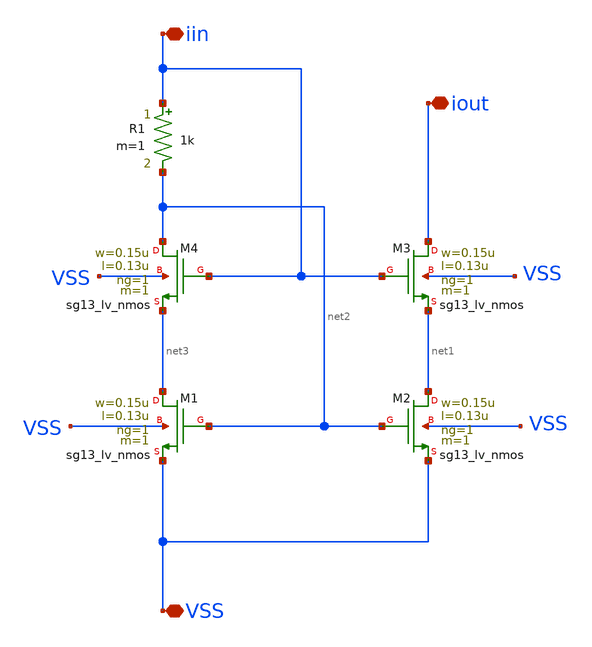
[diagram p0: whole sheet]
** sch_path: analog-db/templates/current_mirror/nmos_current_sink/selfbiased_high_swing_cascode_current_mirror.sch
* Copyright 2026 MacAnalog Research Group
**.subckt selfbiased_high_swing_cascode_current_mirror VSS iin iout
*.iopin VSS
*.iopin iin
*.iopin iout
XM1 net3 net2 VSS VSS sg13_lv_nmos w=0.15u l=0.13u ng=1 m=1 mm_ok=1
XM2 net1 net2 VSS VSS sg13_lv_nmos w=0.15u l=0.13u ng=1 m=1 mm_ok=1
XM3 iout iin net1 VSS sg13_lv_nmos w=0.15u l=0.13u ng=1 m=1 mm_ok=1
XM4 net2 iin net3 VSS sg13_lv_nmos w=0.15u l=0.13u ng=1 m=1 mm_ok=1
R1 iin net2 1k m=1
**.ends
.end
